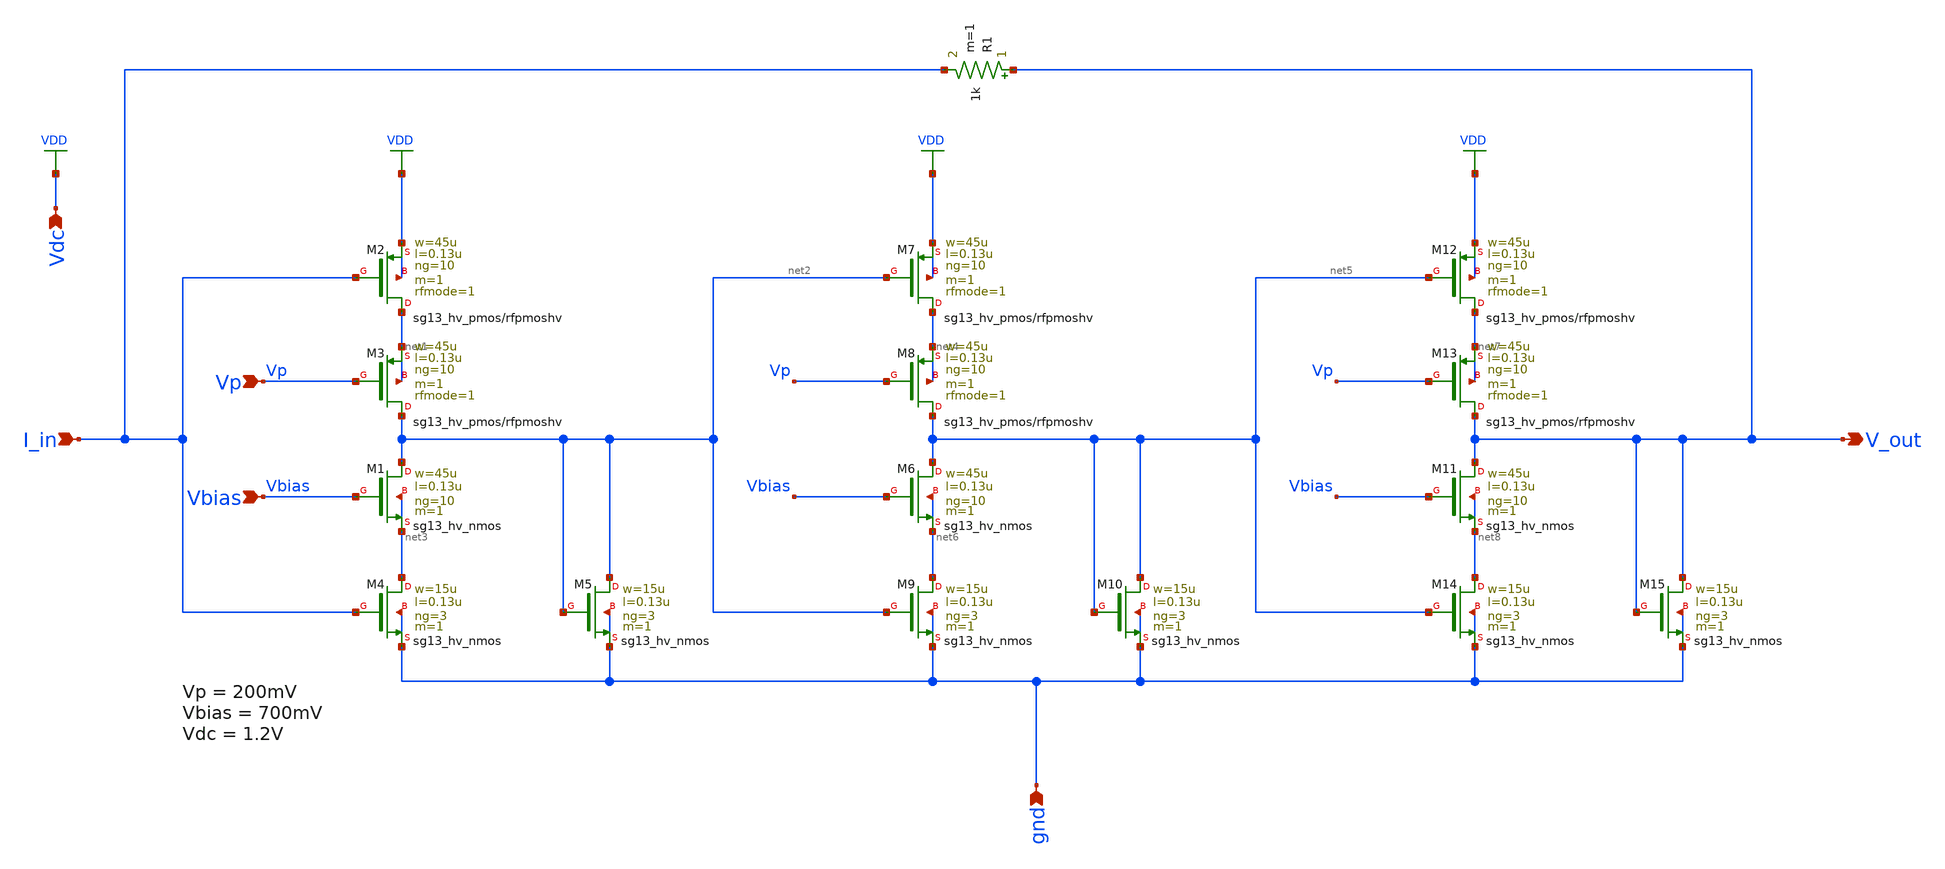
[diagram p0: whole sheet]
** sch_path: TIA_LSI/TIA_50GHz/design_data/xschem/schematic_50G_TIA.sch
* Copyright 2023 IHP PDK Authors
* Licensed under the Apache License, Version 2.0 (the "License");
* you may not use this file except in compliance with the License.
* You may obtain a copy of the License at
* https://www.apache.org/licenses/LICENSE-2.0
* Unless required by applicable law or agreed to in writing, software
* distributed under the License is distributed on an "AS IS" BASIS,
* WITHOUT WARRANTIES OR CONDITIONS OF ANY KIND, either express or implied.
* See the License for the specific language governing permissions and
* limitations under the License.
**.subckt schematic_50G_TIA Vp Vbias I_in gnd Vdc V_out
*.ipin Vp
*.ipin Vbias
*.ipin I_in
*.ipin gnd
*.ipin Vdc
*.opin V_out
XM1 net2 Vbias net3 net3 sg13_hv_nmos w=45u l=0.13u ng=10 m=1 mm_ok=1
XM2 net1 I_in VDD VDD sg13_hv_pmos w=45u l=0.13u ng=10 m=1 rfmode=1 mm_ok=1
R1 V_out I_in 1k m=1
XM3 net2 Vp net1 net1 sg13_hv_pmos w=45u l=0.13u ng=10 m=1 rfmode=1 mm_ok=1
XM4 net3 I_in gnd gnd sg13_hv_nmos w=15u l=0.13u ng=3 m=1 mm_ok=1
XM5 net2 net2 gnd gnd sg13_hv_nmos w=15u l=0.13u ng=3 m=1 mm_ok=1
XM6 net5 Vbias net6 net6 sg13_hv_nmos w=45u l=0.13u ng=10 m=1 mm_ok=1
XM7 net4 net2 VDD VDD sg13_hv_pmos w=45u l=0.13u ng=10 m=1 rfmode=1 mm_ok=1
XM8 net5 Vp net4 net4 sg13_hv_pmos w=45u l=0.13u ng=10 m=1 rfmode=1 mm_ok=1
XM9 net6 net2 gnd gnd sg13_hv_nmos w=15u l=0.13u ng=3 m=1 mm_ok=1
XM10 net5 net5 gnd gnd sg13_hv_nmos w=15u l=0.13u ng=3 m=1 mm_ok=1
XM11 V_out Vbias net8 net8 sg13_hv_nmos w=45u l=0.13u ng=10 m=1 mm_ok=1
XM12 net7 net5 VDD VDD sg13_hv_pmos w=45u l=0.13u ng=10 m=1 rfmode=1 mm_ok=1
XM13 V_out Vp net7 net7 sg13_hv_pmos w=45u l=0.13u ng=10 m=1 rfmode=1 mm_ok=1
XM14 net8 net5 gnd gnd sg13_hv_nmos w=15u l=0.13u ng=3 m=1 mm_ok=1
XM15 V_out V_out gnd gnd sg13_hv_nmos w=15u l=0.13u ng=3 m=1 mm_ok=1
**.ends
.GLOBAL VDD
.end
